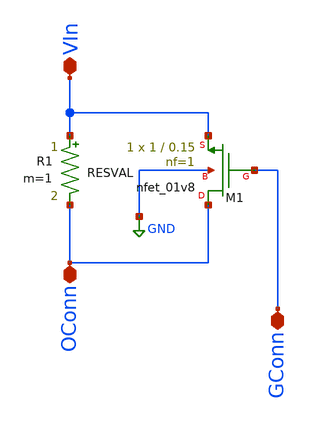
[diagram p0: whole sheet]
** sch_path: xschem_work/Crossbar/nmos_res.sch
**.subckt nmos_res VIn OConn GConn
*.iopin VIn
*.iopin OConn
*.iopin GConn
R1 VIn OConn RESVAL m=1
XM1 OConn GConn VIn GND sky130_fd_pr__nfet_01v8 L=0.15 W=1 nf=1 ad='int((nf+1)/2) * W/nf * 0.29' as='int((nf+2)/2) * W/nf * 0.29'
+ pd='2*int((nf+1)/2) * (W/nf + 0.29)' ps='2*int((nf+2)/2) * (W/nf + 0.29)' nrd='0.29 / W' nrs='0.29 / W'
+ sa=0 sb=0 sd=0 mult=1 m=1
**.ends
.GLOBAL GND
.end
